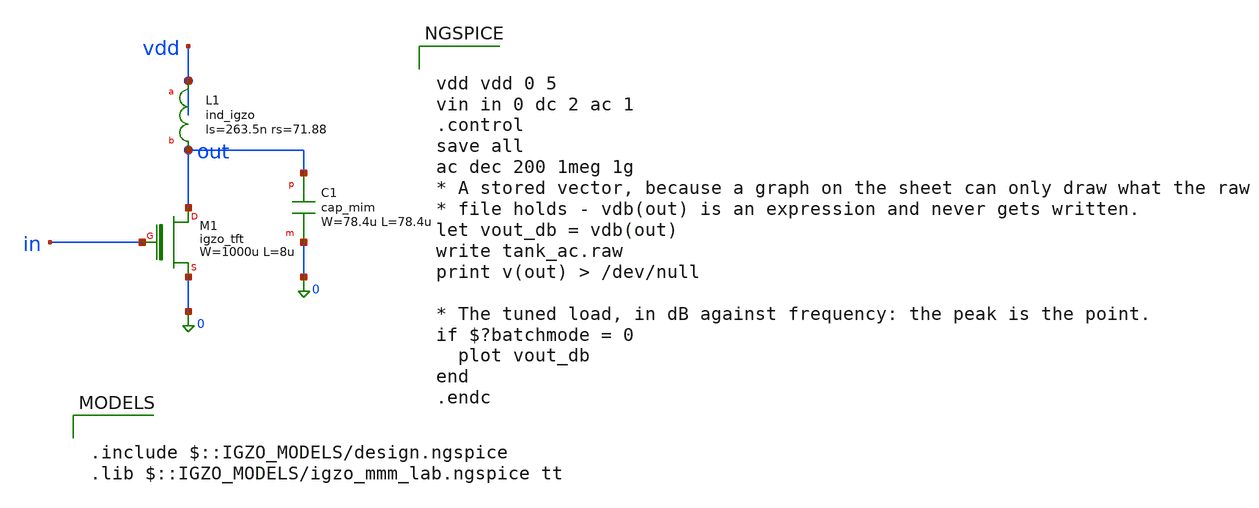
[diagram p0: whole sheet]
** sch_path: libs.tech/xschem/tests/tank_ac.sch
**.subckt tank_ac
XM1 out in 0 igzo_tft W=1000u L=8u ov=5u nf=1 m=1
XL1 vdd out ind_igzo ls=263.5n rs=71.88
XC1 out 0 cap_mim W=78.4u L=78.4u
**** begin user architecture code

.include $::IGZO_MODELS/design.ngspice
.lib $::IGZO_MODELS/igzo_mmm_lab.ngspice tt



vdd vdd 0 5
vin in 0 dc 2 ac 1
.control
save all
ac dec 200 1meg 1g
* A stored vector, because a graph on the sheet can only draw what the raw
* file holds - vdb(out) is an expression and never gets written.
let vout_db = vdb(out)
write tank_ac.raw
print v(out) > /dev/null

* The tuned load, in dB against frequency: the peak is the point.
if $?batchmode = 0
  plot vout_db
end
.endc


**** end user architecture code
**.ends
.end
